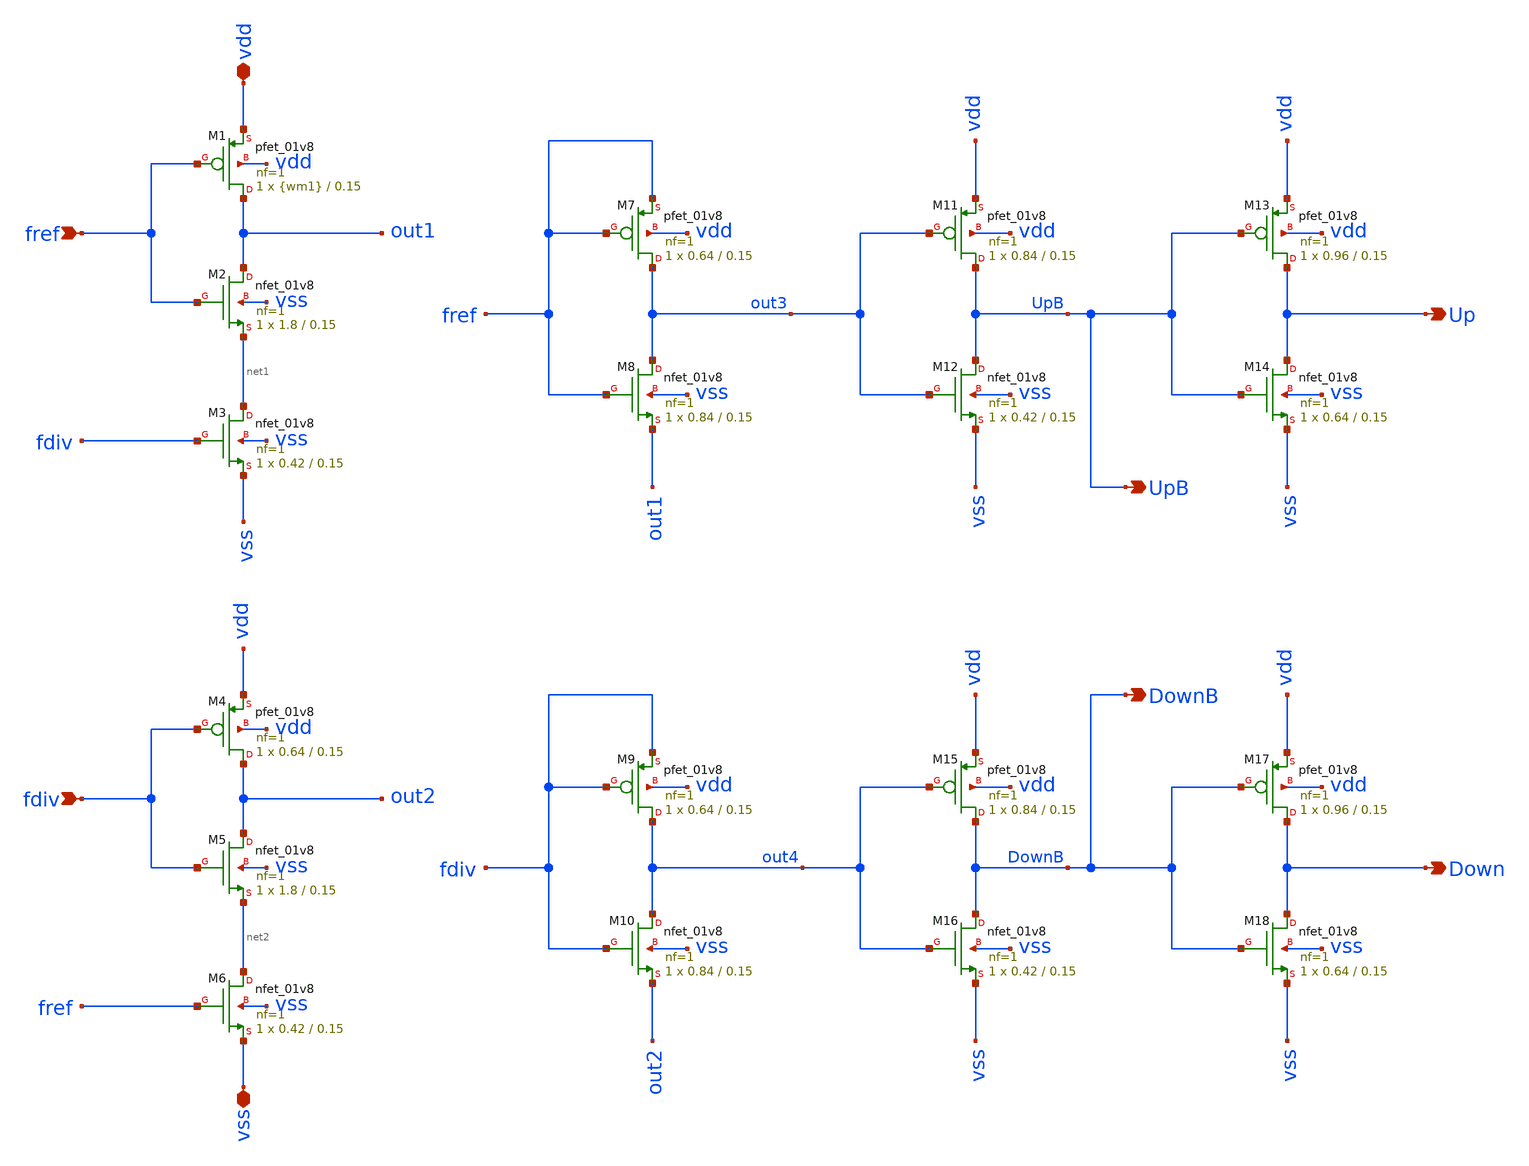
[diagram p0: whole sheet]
** sch_path: sch/PLL_caravel/PFD.sch
**.subckt PFD fref vdd Down fdiv vss Up UpB DownB
*.ipin fref
*.iopin vdd
*.opin Down
*.ipin fdiv
*.iopin vss
*.opin Up
*.opin UpB
*.opin DownB
XM1 out1 fref vdd vdd sky130_fd_pr__pfet_01v8 L=0.15 W={wm1} nf=1 ad='int((nf+1)/2) * W/nf * 0.29' as='int((nf+2)/2) * W/nf * 0.29'
+ pd='2*int((nf+1)/2) * (W/nf + 0.29)' ps='2*int((nf+2)/2) * (W/nf + 0.29)' nrd='0.29 / W' nrs='0.29 / W'
+ sa=0 sb=0 sd=0 mult=1 m=1
XM2 out1 fref net1 vss sky130_fd_pr__nfet_01v8 L=0.15 W=1.8 nf=1 ad='int((nf+1)/2) * W/nf * 0.29' as='int((nf+2)/2) * W/nf * 0.29'
+ pd='2*int((nf+1)/2) * (W/nf + 0.29)' ps='2*int((nf+2)/2) * (W/nf + 0.29)' nrd='0.29 / W' nrs='0.29 / W'
+ sa=0 sb=0 sd=0 mult=1 m=1
XM3 net1 fdiv vss vss sky130_fd_pr__nfet_01v8 L=0.15 W=0.42 nf=1 ad='int((nf+1)/2) * W/nf * 0.29' as='int((nf+2)/2) * W/nf * 0.29'
+ pd='2*int((nf+1)/2) * (W/nf + 0.29)' ps='2*int((nf+2)/2) * (W/nf + 0.29)' nrd='0.29 / W' nrs='0.29 / W'
+ sa=0 sb=0 sd=0 mult=1 m=1
XM4 out2 fdiv vdd vdd sky130_fd_pr__pfet_01v8 L=0.15 W=0.64 nf=1 ad='int((nf+1)/2) * W/nf * 0.29' as='int((nf+2)/2) * W/nf * 0.29'
+ pd='2*int((nf+1)/2) * (W/nf + 0.29)' ps='2*int((nf+2)/2) * (W/nf + 0.29)' nrd='0.29 / W' nrs='0.29 / W'
+ sa=0 sb=0 sd=0 mult=1 m=1
XM5 out2 fdiv net2 vss sky130_fd_pr__nfet_01v8 L=0.15 W=1.8 nf=1 ad='int((nf+1)/2) * W/nf * 0.29' as='int((nf+2)/2) * W/nf * 0.29'
+ pd='2*int((nf+1)/2) * (W/nf + 0.29)' ps='2*int((nf+2)/2) * (W/nf + 0.29)' nrd='0.29 / W' nrs='0.29 / W'
+ sa=0 sb=0 sd=0 mult=1 m=1
XM6 net2 fref vss vss sky130_fd_pr__nfet_01v8 L=0.15 W=0.42 nf=1 ad='int((nf+1)/2) * W/nf * 0.29' as='int((nf+2)/2) * W/nf * 0.29'
+ pd='2*int((nf+1)/2) * (W/nf + 0.29)' ps='2*int((nf+2)/2) * (W/nf + 0.29)' nrd='0.29 / W' nrs='0.29 / W'
+ sa=0 sb=0 sd=0 mult=1 m=1
XM7 out3 fref fref vdd sky130_fd_pr__pfet_01v8 L=0.15 W=0.64 nf=1 ad='int((nf+1)/2) * W/nf * 0.29' as='int((nf+2)/2) * W/nf * 0.29'
+ pd='2*int((nf+1)/2) * (W/nf + 0.29)' ps='2*int((nf+2)/2) * (W/nf + 0.29)' nrd='0.29 / W' nrs='0.29 / W'
+ sa=0 sb=0 sd=0 mult=1 m=1
XM8 out3 fref out1 vss sky130_fd_pr__nfet_01v8 L=0.15 W=0.84 nf=1 ad='int((nf+1)/2) * W/nf * 0.29' as='int((nf+2)/2) * W/nf * 0.29'
+ pd='2*int((nf+1)/2) * (W/nf + 0.29)' ps='2*int((nf+2)/2) * (W/nf + 0.29)' nrd='0.29 / W' nrs='0.29 / W'
+ sa=0 sb=0 sd=0 mult=1 m=1
XM9 out4 fdiv fdiv vdd sky130_fd_pr__pfet_01v8 L=0.15 W=0.64 nf=1 ad='int((nf+1)/2) * W/nf * 0.29' as='int((nf+2)/2) * W/nf * 0.29'
+ pd='2*int((nf+1)/2) * (W/nf + 0.29)' ps='2*int((nf+2)/2) * (W/nf + 0.29)' nrd='0.29 / W' nrs='0.29 / W'
+ sa=0 sb=0 sd=0 mult=1 m=1
XM10 out4 fdiv out2 vss sky130_fd_pr__nfet_01v8 L=0.15 W=0.84 nf=1 ad='int((nf+1)/2) * W/nf * 0.29' as='int((nf+2)/2) * W/nf * 0.29'
+ pd='2*int((nf+1)/2) * (W/nf + 0.29)' ps='2*int((nf+2)/2) * (W/nf + 0.29)' nrd='0.29 / W' nrs='0.29 / W'
+ sa=0 sb=0 sd=0 mult=1 m=1
XM11 UpB out3 vdd vdd sky130_fd_pr__pfet_01v8 L=0.15 W=0.84 nf=1 ad='int((nf+1)/2) * W/nf * 0.29' as='int((nf+2)/2) * W/nf * 0.29'
+ pd='2*int((nf+1)/2) * (W/nf + 0.29)' ps='2*int((nf+2)/2) * (W/nf + 0.29)' nrd='0.29 / W' nrs='0.29 / W'
+ sa=0 sb=0 sd=0 mult=1 m=1
XM12 UpB out3 vss vss sky130_fd_pr__nfet_01v8 L=0.15 W=0.42 nf=1 ad='int((nf+1)/2) * W/nf * 0.29' as='int((nf+2)/2) * W/nf * 0.29'
+ pd='2*int((nf+1)/2) * (W/nf + 0.29)' ps='2*int((nf+2)/2) * (W/nf + 0.29)' nrd='0.29 / W' nrs='0.29 / W'
+ sa=0 sb=0 sd=0 mult=1 m=1
XM13 Up UpB vdd vdd sky130_fd_pr__pfet_01v8 L=0.15 W=0.96 nf=1 ad='int((nf+1)/2) * W/nf * 0.29' as='int((nf+2)/2) * W/nf * 0.29'
+ pd='2*int((nf+1)/2) * (W/nf + 0.29)' ps='2*int((nf+2)/2) * (W/nf + 0.29)' nrd='0.29 / W' nrs='0.29 / W'
+ sa=0 sb=0 sd=0 mult=1 m=1
XM14 Up UpB vss vss sky130_fd_pr__nfet_01v8 L=0.15 W=0.64 nf=1 ad='int((nf+1)/2) * W/nf * 0.29' as='int((nf+2)/2) * W/nf * 0.29'
+ pd='2*int((nf+1)/2) * (W/nf + 0.29)' ps='2*int((nf+2)/2) * (W/nf + 0.29)' nrd='0.29 / W' nrs='0.29 / W'
+ sa=0 sb=0 sd=0 mult=1 m=1
XM15 DownB out4 vdd vdd sky130_fd_pr__pfet_01v8 L=0.15 W=0.84 nf=1 ad='int((nf+1)/2) * W/nf * 0.29' as='int((nf+2)/2) * W/nf * 0.29'
+ pd='2*int((nf+1)/2) * (W/nf + 0.29)' ps='2*int((nf+2)/2) * (W/nf + 0.29)' nrd='0.29 / W' nrs='0.29 / W'
+ sa=0 sb=0 sd=0 mult=1 m=1
XM16 DownB out4 vss vss sky130_fd_pr__nfet_01v8 L=0.15 W=0.42 nf=1 ad='int((nf+1)/2) * W/nf * 0.29' as='int((nf+2)/2) * W/nf * 0.29'
+ pd='2*int((nf+1)/2) * (W/nf + 0.29)' ps='2*int((nf+2)/2) * (W/nf + 0.29)' nrd='0.29 / W' nrs='0.29 / W'
+ sa=0 sb=0 sd=0 mult=1 m=1
XM17 Down DownB vdd vdd sky130_fd_pr__pfet_01v8 L=0.15 W=0.96 nf=1 ad='int((nf+1)/2) * W/nf * 0.29' as='int((nf+2)/2) * W/nf * 0.29'
+ pd='2*int((nf+1)/2) * (W/nf + 0.29)' ps='2*int((nf+2)/2) * (W/nf + 0.29)' nrd='0.29 / W' nrs='0.29 / W'
+ sa=0 sb=0 sd=0 mult=1 m=1
XM18 Down DownB vss vss sky130_fd_pr__nfet_01v8 L=0.15 W=0.64 nf=1 ad='int((nf+1)/2) * W/nf * 0.29' as='int((nf+2)/2) * W/nf * 0.29'
+ pd='2*int((nf+1)/2) * (W/nf + 0.29)' ps='2*int((nf+2)/2) * (W/nf + 0.29)' nrd='0.29 / W' nrs='0.29 / W'
+ sa=0 sb=0 sd=0 mult=1 m=1
**.ends
.end
